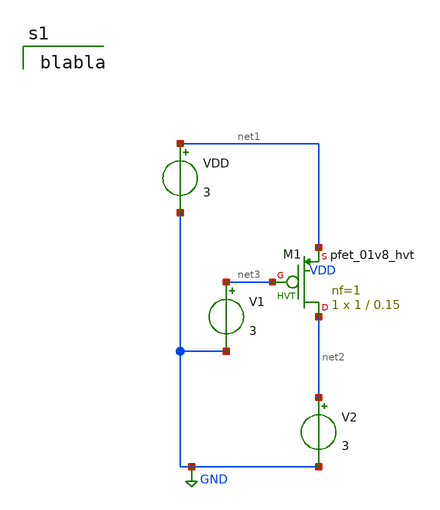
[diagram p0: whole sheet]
** sch_path: schematics/hvt_pmos_char.sch
**.subckt hvt_pmos_char
XM1 net2 net3 net1 VDD sky130_fd_pr__pfet_01v8_hvt L=0.15 W=1 nf=1 ad='int((nf+1)/2) * W/nf * 0.29' as='int((nf+2)/2) * W/nf * 0.29'
+ pd='2*int((nf+1)/2) * (W/nf + 0.29)' ps='2*int((nf+2)/2) * (W/nf + 0.29)' nrd='0.29 / W' nrs='0.29 / W'
+ sa=0 sb=0 sd=0 mult=1 m=1
V1 net3 GND 3
V2 net2 GND 3
VDD net1 GND 3
**** begin user architecture code

blabla

**** end user architecture code
**.ends
.GLOBAL GND
.end
